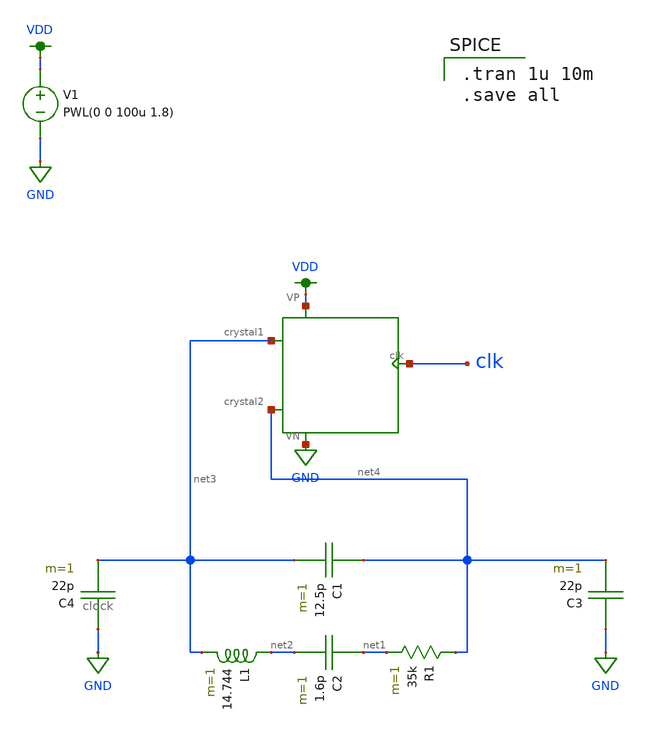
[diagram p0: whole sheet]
** sch_path: analog/osc.sch
**.subckt osc
C1 net4 net3 12.5p m=1
L1 net2 net3 14.744 m=1
C2 net1 net2 1.6p m=1
R1 net4 net1 35k m=1
V1 VDD GND PWL(0 0 100u 1.8)
X1 net3 net4 clk VDD GND clock
C3 GND net4 22p m=1
C4 GND net3 22p m=1
**** begin user architecture code

.tran 1u 10m
.save all


.option wnflag=1
.param MC_SWITCH=0.0
.lib ~/skywater/skywater-pdk/libraries/sky130_fd_pr_ngspice/latest/models/sky130.lib.spice tt

**** end user architecture code
**.ends
.GLOBAL VDD
.GLOBAL GND
.end
